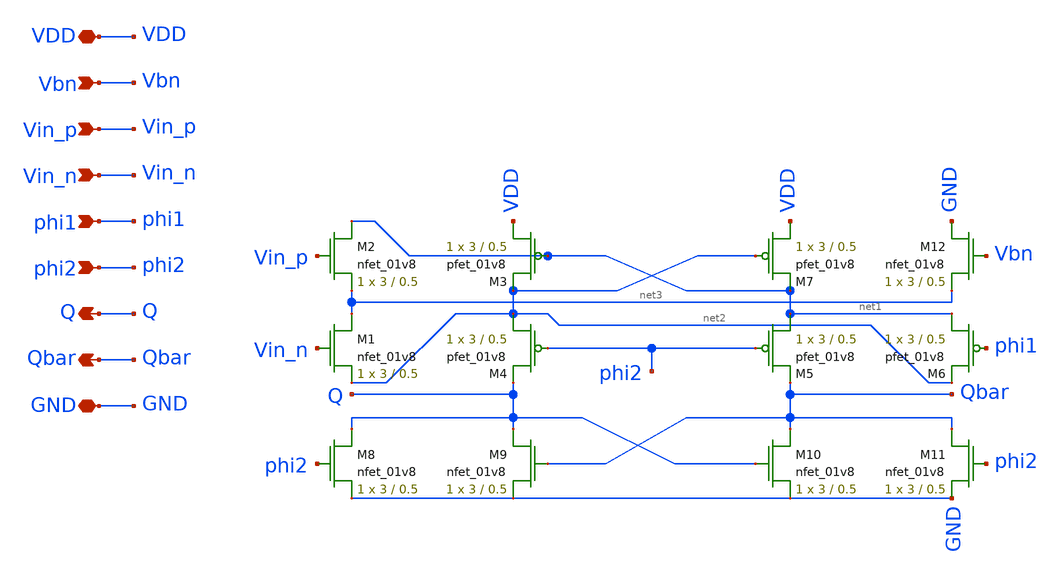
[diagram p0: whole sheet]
** sch_path: final/LDS/comparator_LDS.sch
**.subckt comparator_LDS Vin_p Vin_n Vbn phi1 phi2 Q Qbar VDD GND
*.ipin Vin_p
*.ipin Vin_n
*.ipin Vbn
*.ipin phi1
*.ipin phi2
*.opin Q
*.opin Qbar
*.iopin VDD
*.iopin GND
XM2 net1 Vin_p net3 GND sky130_fd_pr__nfet_01v8 L=0.5 W=3 nf=1 ad='int((nf+1)/2) * W/nf * 0.29' as='int((nf+2)/2) * W/nf * 0.29'
+ pd='2*int((nf+1)/2) * (W/nf + 0.29)' ps='2*int((nf+2)/2) * (W/nf + 0.29)' nrd='0.29 / W' nrs='0.29 / W'
+ sa=0 sb=0 sd=0 mult=1 m=1
XM3 VDD net1 net2 VDD sky130_fd_pr__pfet_01v8 L=0.5 W=3 nf=1 ad='int((nf+1)/2) * W/nf * 0.29' as='int((nf+2)/2) * W/nf * 0.29'
+ pd='2*int((nf+1)/2) * (W/nf + 0.29)' ps='2*int((nf+2)/2) * (W/nf + 0.29)' nrd='0.29 / W' nrs='0.29 / W'
+ sa=0 sb=0 sd=0 mult=1 m=1
XM1 net3 Vin_n net2 GND sky130_fd_pr__nfet_01v8 L=0.5 W=3 nf=1 ad='int((nf+1)/2) * W/nf * 0.29' as='int((nf+2)/2) * W/nf * 0.29'
+ pd='2*int((nf+1)/2) * (W/nf + 0.29)' ps='2*int((nf+2)/2) * (W/nf + 0.29)' nrd='0.29 / W' nrs='0.29 / W'
+ sa=0 sb=0 sd=0 mult=1 m=1
XM8 Q phi2 GND GND sky130_fd_pr__nfet_01v8 L=0.5 W=3 nf=1 ad='int((nf+1)/2) * W/nf * 0.29' as='int((nf+2)/2) * W/nf * 0.29'
+ pd='2*int((nf+1)/2) * (W/nf + 0.29)' ps='2*int((nf+2)/2) * (W/nf + 0.29)' nrd='0.29 / W' nrs='0.29 / W'
+ sa=0 sb=0 sd=0 mult=1 m=1
XM9 Q Qbar GND GND sky130_fd_pr__nfet_01v8 L=0.5 W=3 nf=1 ad='int((nf+1)/2) * W/nf * 0.29' as='int((nf+2)/2) * W/nf * 0.29'
+ pd='2*int((nf+1)/2) * (W/nf + 0.29)' ps='2*int((nf+2)/2) * (W/nf + 0.29)' nrd='0.29 / W' nrs='0.29 / W'
+ sa=0 sb=0 sd=0 mult=1 m=1
XM10 Qbar Q GND GND sky130_fd_pr__nfet_01v8 L=0.5 W=3 nf=1 ad='int((nf+1)/2) * W/nf * 0.29' as='int((nf+2)/2) * W/nf * 0.29'
+ pd='2*int((nf+1)/2) * (W/nf + 0.29)' ps='2*int((nf+2)/2) * (W/nf + 0.29)' nrd='0.29 / W' nrs='0.29 / W'
+ sa=0 sb=0 sd=0 mult=1 m=1
XM11 Qbar phi2 GND GND sky130_fd_pr__nfet_01v8 L=0.5 W=3 nf=1 ad='int((nf+1)/2) * W/nf * 0.29' as='int((nf+2)/2) * W/nf * 0.29'
+ pd='2*int((nf+1)/2) * (W/nf + 0.29)' ps='2*int((nf+2)/2) * (W/nf + 0.29)' nrd='0.29 / W' nrs='0.29 / W'
+ sa=0 sb=0 sd=0 mult=1 m=1
XM12 GND Vbn net3 GND sky130_fd_pr__nfet_01v8 L=0.5 W=3 nf=1 ad='int((nf+1)/2) * W/nf * 0.29' as='int((nf+2)/2) * W/nf * 0.29'
+ pd='2*int((nf+1)/2) * (W/nf + 0.29)' ps='2*int((nf+2)/2) * (W/nf + 0.29)' nrd='0.29 / W' nrs='0.29 / W'
+ sa=0 sb=0 sd=0 mult=1 m=1
XM4 net2 phi2 Q VDD sky130_fd_pr__pfet_01v8 L=0.5 W=3 nf=1 ad='int((nf+1)/2) * W/nf * 0.29' as='int((nf+2)/2) * W/nf * 0.29'
+ pd='2*int((nf+1)/2) * (W/nf + 0.29)' ps='2*int((nf+2)/2) * (W/nf + 0.29)' nrd='0.29 / W' nrs='0.29 / W'
+ sa=0 sb=0 sd=0 mult=1 m=1
XM5 net1 phi2 Qbar VDD sky130_fd_pr__pfet_01v8 L=0.5 W=3 nf=1 ad='int((nf+1)/2) * W/nf * 0.29' as='int((nf+2)/2) * W/nf * 0.29'
+ pd='2*int((nf+1)/2) * (W/nf + 0.29)' ps='2*int((nf+2)/2) * (W/nf + 0.29)' nrd='0.29 / W' nrs='0.29 / W'
+ sa=0 sb=0 sd=0 mult=1 m=1
XM6 net1 phi1 net2 VDD sky130_fd_pr__pfet_01v8 L=0.5 W=3 nf=1 ad='int((nf+1)/2) * W/nf * 0.29' as='int((nf+2)/2) * W/nf * 0.29'
+ pd='2*int((nf+1)/2) * (W/nf + 0.29)' ps='2*int((nf+2)/2) * (W/nf + 0.29)' nrd='0.29 / W' nrs='0.29 / W'
+ sa=0 sb=0 sd=0 mult=1 m=1
XM7 VDD net2 net1 VDD sky130_fd_pr__pfet_01v8 L=0.5 W=3 nf=1 ad='int((nf+1)/2) * W/nf * 0.29' as='int((nf+2)/2) * W/nf * 0.29'
+ pd='2*int((nf+1)/2) * (W/nf + 0.29)' ps='2*int((nf+2)/2) * (W/nf + 0.29)' nrd='0.29 / W' nrs='0.29 / W'
+ sa=0 sb=0 sd=0 mult=1 m=1
**.ends
.end
